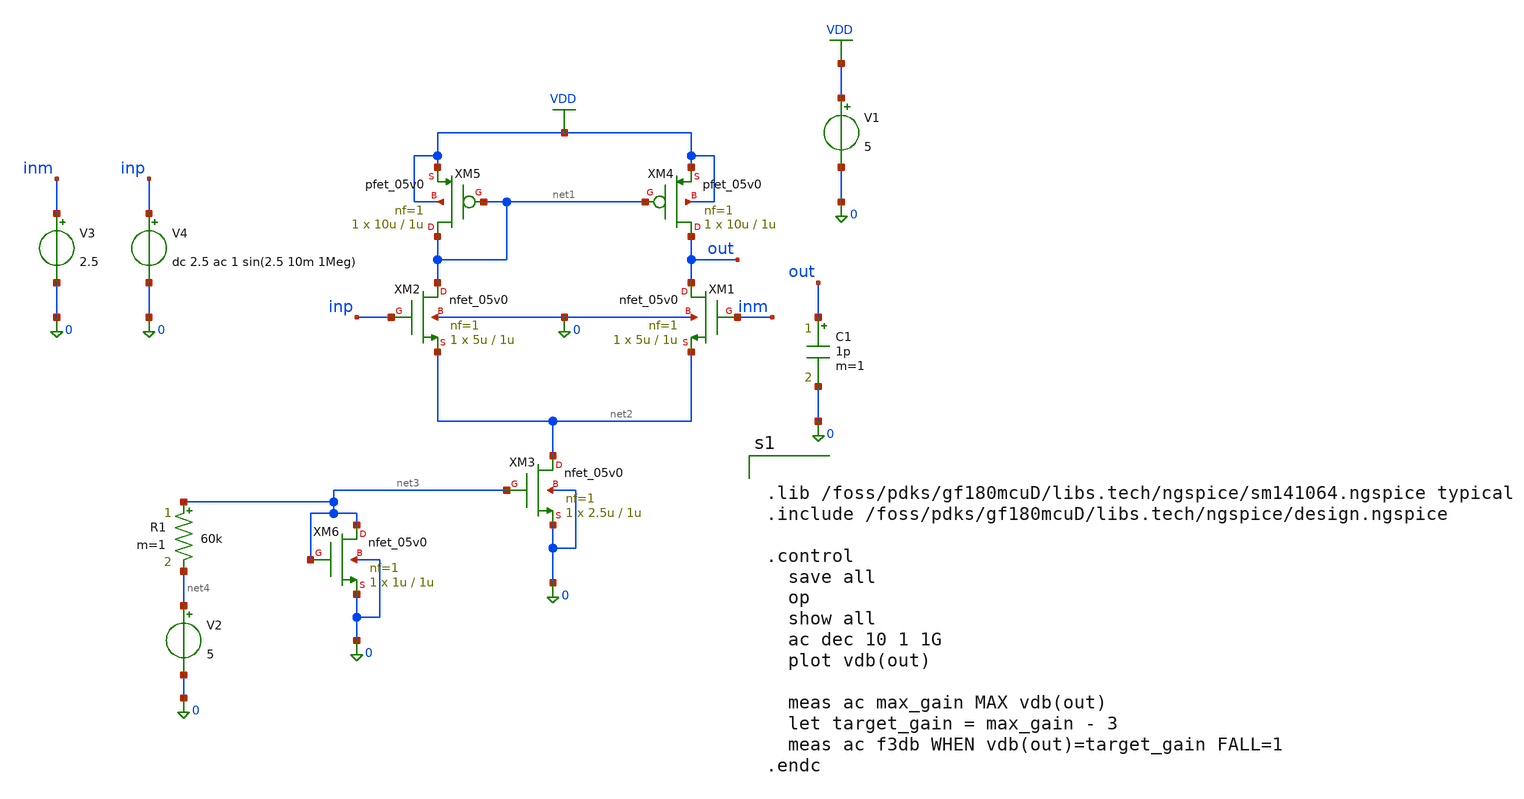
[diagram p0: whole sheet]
** sch_path: testcircuit.sch
**.subckt testcircuit
XM1 out inm net2 0 nfet_05v0 L=1u W=5u nf=1 ad='int((nf+1)/2) * W/nf * 0.18u' as='int((nf+2)/2) * W/nf * 0.18u'
+ pd='2*int((nf+1)/2) * (W/nf + 0.18u)' ps='2*int((nf+2)/2) * (W/nf + 0.18u)' nrd='0.18u / W' nrs='0.18u / W'
+ sa=0 sb=0 sd=0 m=1
XM2 net1 inp net2 0 nfet_05v0 L=1u W=5u nf=1 ad='int((nf+1)/2) * W/nf * 0.18u' as='int((nf+2)/2) * W/nf * 0.18u'
+ pd='2*int((nf+1)/2) * (W/nf + 0.18u)' ps='2*int((nf+2)/2) * (W/nf + 0.18u)' nrd='0.18u / W' nrs='0.18u / W'
+ sa=0 sb=0 sd=0 m=1
XM3 net2 net3 0 0 nfet_05v0 L=1u W=2.5u nf=1 ad='int((nf+1)/2) * W/nf * 0.18u' as='int((nf+2)/2) * W/nf * 0.18u'
+ pd='2*int((nf+1)/2) * (W/nf + 0.18u)' ps='2*int((nf+2)/2) * (W/nf + 0.18u)' nrd='0.18u / W' nrs='0.18u / W'
+ sa=0 sb=0 sd=0 m=1
XM4 out net1 VDD VDD pfet_05v0 L=1u W=10u nf=1 ad='int((nf+1)/2) * W/nf * 0.18u' as='int((nf+2)/2) * W/nf * 0.18u'
+ pd='2*int((nf+1)/2) * (W/nf + 0.18u)' ps='2*int((nf+2)/2) * (W/nf + 0.18u)' nrd='0.18u / W' nrs='0.18u / W'
+ sa=0 sb=0 sd=0 m=1
XM5 net1 net1 VDD VDD pfet_05v0 L=1u W=10u nf=1 ad='int((nf+1)/2) * W/nf * 0.18u' as='int((nf+2)/2) * W/nf * 0.18u'
+ pd='2*int((nf+1)/2) * (W/nf + 0.18u)' ps='2*int((nf+2)/2) * (W/nf + 0.18u)' nrd='0.18u / W' nrs='0.18u / W'
+ sa=0 sb=0 sd=0 m=1
V1 VDD 0 5
V3 inm 0 2.5
V4 inp 0 dc 2.5 ac 1 sin(2.5 10m 1Meg)
C1 out 0 1p m=1
XM6 net3 net3 0 0 nfet_05v0 L=1u W=1u nf=1 ad='int((nf+1)/2) * W/nf * 0.18u' as='int((nf+2)/2) * W/nf * 0.18u'
+ pd='2*int((nf+1)/2) * (W/nf + 0.18u)' ps='2*int((nf+2)/2) * (W/nf + 0.18u)' nrd='0.18u / W' nrs='0.18u / W'
+ sa=0 sb=0 sd=0 m=1
R1 net3 net4 60k m=1
V2 net4 0 5
**** begin user architecture code


.lib /foss/pdks/gf180mcuD/libs.tech/ngspice/sm141064.ngspice typical
.include /foss/pdks/gf180mcuD/libs.tech/ngspice/design.ngspice

.control
  save all
  op
  show all
  ac dec 10 1 1G
  plot vdb(out)

  meas ac max_gain MAX vdb(out)
  let target_gain = max_gain - 3
  meas ac f3db WHEN vdb(out)=target_gain FALL=1
.endc


**** end user architecture code
**.ends
.GLOBAL VDD
.end
